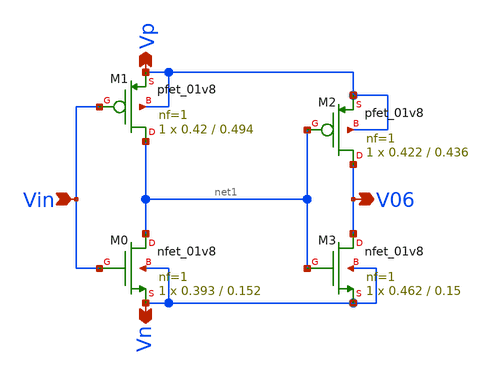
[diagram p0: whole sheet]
** sch_path: xschem/Vth_sch/Symbol/th06.sch
**.subckt th06 Vn Vp Vin V06
*.opin Vn
*.opin Vp
*.ipin Vin
*.opin V06
XM2 V06 net1 Vp Vp sky130_fd_pr__pfet_01v8 L=0.436 W=0.422 nf=1 ad='int((nf+1)/2) * W/nf * 0.29' as='int((nf+2)/2) * W/nf * 0.29'
+ pd='2*int((nf+1)/2) * (W/nf + 0.29)' ps='2*int((nf+2)/2) * (W/nf + 0.29)' nrd='0.29 / W' nrs='0.29 / W'
+ sa=0 sb=0 sd=0 mult=1 m=1
XM3 V06 net1 Vn Vn sky130_fd_pr__nfet_01v8 L=0.15 W=0.462 nf=1 ad='int((nf+1)/2) * W/nf * 0.29' as='int((nf+2)/2) * W/nf * 0.29'
+ pd='2*int((nf+1)/2) * (W/nf + 0.29)' ps='2*int((nf+2)/2) * (W/nf + 0.29)' nrd='0.29 / W' nrs='0.29 / W'
+ sa=0 sb=0 sd=0 mult=1 m=1
XM1 net1 Vin Vp Vp sky130_fd_pr__pfet_01v8 L=0.494 W=0.42 nf=1 ad='int((nf+1)/2) * W/nf * 0.29' as='int((nf+2)/2) * W/nf * 0.29'
+ pd='2*int((nf+1)/2) * (W/nf + 0.29)' ps='2*int((nf+2)/2) * (W/nf + 0.29)' nrd='0.29 / W' nrs='0.29 / W'
+ sa=0 sb=0 sd=0 mult=1 m=1
XM0 net1 Vin Vn Vn sky130_fd_pr__nfet_01v8 L=0.152 W=0.393 nf=1 ad='int((nf+1)/2) * W/nf * 0.29' as='int((nf+2)/2) * W/nf * 0.29'
+ pd='2*int((nf+1)/2) * (W/nf + 0.29)' ps='2*int((nf+2)/2) * (W/nf + 0.29)' nrd='0.29 / W' nrs='0.29 / W'
+ sa=0 sb=0 sd=0 mult=1 m=1
**.ends
.end
